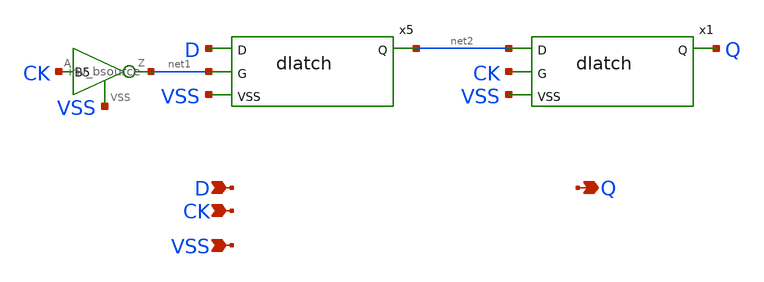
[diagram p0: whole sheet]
** sch_path: xschem-src/xschem_library/examples/flop.sch
* Copyright (C) 1998-2026 Stefan Frederik Schippers
* This program is free software; you can redistribute it and/or modify
* it under the terms of the GNU General Public License as published by
* the Free Software Foundation; either version 2 of the License, or
* (at your option) any later version.
* This program is distributed in the hope that it will be useful,
* but WITHOUT ANY WARRANTY; without even the implied warranty of
* MERCHANTABILITY or FITNESS FOR A PARTICULAR PURPOSE.  See the
* GNU General Public License for more details.
* You should have received a copy of the GNU General Public License
* along with this program; if not, write to the Free Software
**.subckt flop D Q VSS CK
*.ipin D
*.opin Q
*.ipin VSS
*.ipin CK
B5 net1 VSS V=pwl(v( CK , VSS ), 'VTH-0.1' VHI 'VTH+0.1' 0 )
x5 D net2 net1 VSS dlatch VTH=VTH VHI=VHI
x1 net2 Q CK VSS dlatch VTH=VTH VHI=VHI
**.ends

* expanding   symbol:  dlatch.sym # of pins=4
** sym_path: xschem-src/xschem_library/examples/dlatch.sym
** sch_path: xschem-src/xschem_library/examples/dlatch.sch
.subckt dlatch D Q G VSS  VTH=1.5 VHI=3.0
*.ipin D
*.opin Q
*.ipin VSS
*.ipin G
G5 net2 net1 vcr pwl(1) G VSS 'VTH-0.1' 10G 'VTH+0.1' 10
c1 net2 VSS 1p m=1
E5 net1 VSS pwl(1) D VSS 'VTH-0.1' 0 'VTH+0.1' VHI
E1 Q VSS pwl(1) net2 VSS 'VTH-0.1' 0 'VTH+0.1' VHI
.ends

.end
